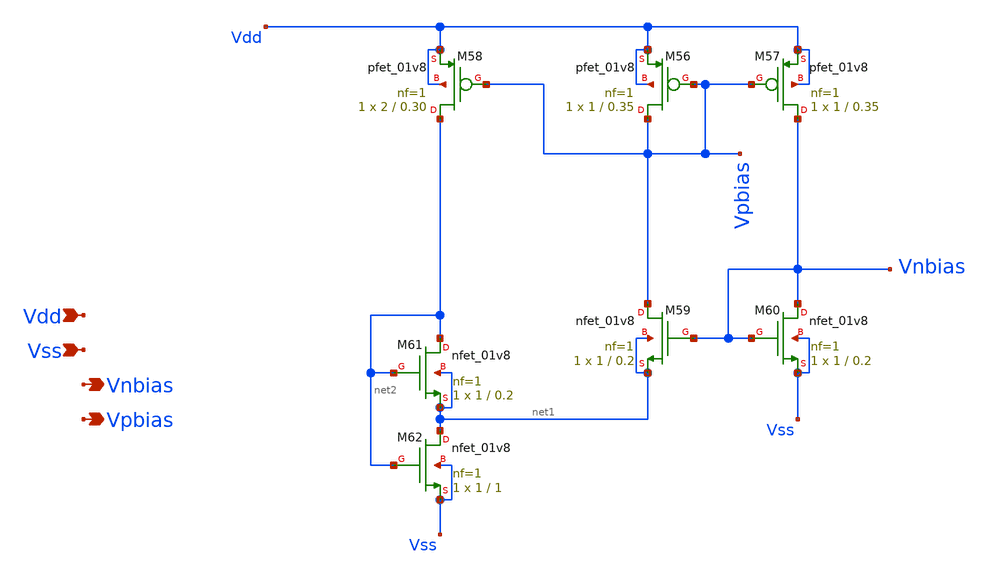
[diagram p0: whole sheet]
** sch_path: tt10-hdl/tt_um_test_commit/xschem/T2/biasGen/Z_old/currSrc_10nA.sch
**.subckt currSrc_10nA Vdd Vss Vnbias Vpbias
*.ipin Vdd
*.ipin Vss
*.opin Vnbias
*.opin Vpbias
XM56 Vpbias Vpbias Vdd Vdd sky130_fd_pr__pfet_01v8 L=0.35 W=1 nf=1 ad='int((nf+1)/2) * W/nf * 0.29' as='int((nf+2)/2) * W/nf * 0.29'
+ pd='2*int((nf+1)/2) * (W/nf + 0.29)' ps='2*int((nf+2)/2) * (W/nf + 0.29)' nrd='0.29 / W' nrs='0.29 / W'
+ sa=0 sb=0 sd=0 mult=1 m=1
XM57 Vnbias Vpbias Vdd Vdd sky130_fd_pr__pfet_01v8 L=0.35 W=1 nf=1 ad='int((nf+1)/2) * W/nf * 0.29' as='int((nf+2)/2) * W/nf * 0.29'
+ pd='2*int((nf+1)/2) * (W/nf + 0.29)' ps='2*int((nf+2)/2) * (W/nf + 0.29)' nrd='0.29 / W' nrs='0.29 / W'
+ sa=0 sb=0 sd=0 mult=1 m=1
XM58 net2 Vpbias Vdd Vdd sky130_fd_pr__pfet_01v8 L=0.30 W=2 nf=1 ad='int((nf+1)/2) * W/nf * 0.29' as='int((nf+2)/2) * W/nf * 0.29'
+ pd='2*int((nf+1)/2) * (W/nf + 0.29)' ps='2*int((nf+2)/2) * (W/nf + 0.29)' nrd='0.29 / W' nrs='0.29 / W'
+ sa=0 sb=0 sd=0 mult=1 m=1
XM59 Vpbias Vnbias net1 net1 sky130_fd_pr__nfet_01v8 L=0.2 W=1 nf=1 ad='int((1 + 1)/2) * 1 / 1 * 0.29'
+ as='int((1 + 2)/2) * 1 / 1 * 0.29' pd='2*int((1 + 1)/2) * (1 / 1 + 0.29)' ps='2*int((1 + 2)/2) * (1 / 1 + 0.29)'
+ nrd='0.29 / 1 ' nrs='0.29 / 1 ' sa=0 sb=0 sd=0 mult=1 m=1
XM60 Vnbias Vnbias Vss Vss sky130_fd_pr__nfet_01v8 L=0.2 W=1 nf=1 ad='int((1 + 1)/2) * 1 / 1 * 0.29'
+ as='int((1 + 2)/2) * 1 / 1 * 0.29' pd='2*int((1 + 1)/2) * (1 / 1 + 0.29)' ps='2*int((1 + 2)/2) * (1 / 1 + 0.29)'
+ nrd='0.29 / 1 ' nrs='0.29 / 1 ' sa=0 sb=0 sd=0 mult=1 m=1
XM61 net2 net2 net1 net1 sky130_fd_pr__nfet_01v8 L=0.2 W=1 nf=1 ad='int((1 + 1)/2) * 1 / 1 * 0.29' as='int((1 + 2)/2) * 1 / 1 * 0.29'
+ pd='2*int((1 + 1)/2) * (1 / 1 + 0.29)' ps='2*int((1 + 2)/2) * (1 / 1 + 0.29)' nrd='0.29 / 1 ' nrs='0.29 / 1 '
+ sa=0 sb=0 sd=0 mult=1 m=1
XM62 net1 net2 Vss Vss sky130_fd_pr__nfet_01v8 L=1 W=1 nf=1 ad='int((1 + 1)/2) * 1 / 1 * 0.29' as='int((1 + 2)/2) * 1 / 1 * 0.29'
+ pd='2*int((1 + 1)/2) * (1 / 1 + 0.29)' ps='2*int((1 + 2)/2) * (1 / 1 + 0.29)' nrd='0.29 / 1 ' nrs='0.29 / 1 '
+ sa=0 sb=0 sd=0 mult=1 m=1
**.ends
.end
